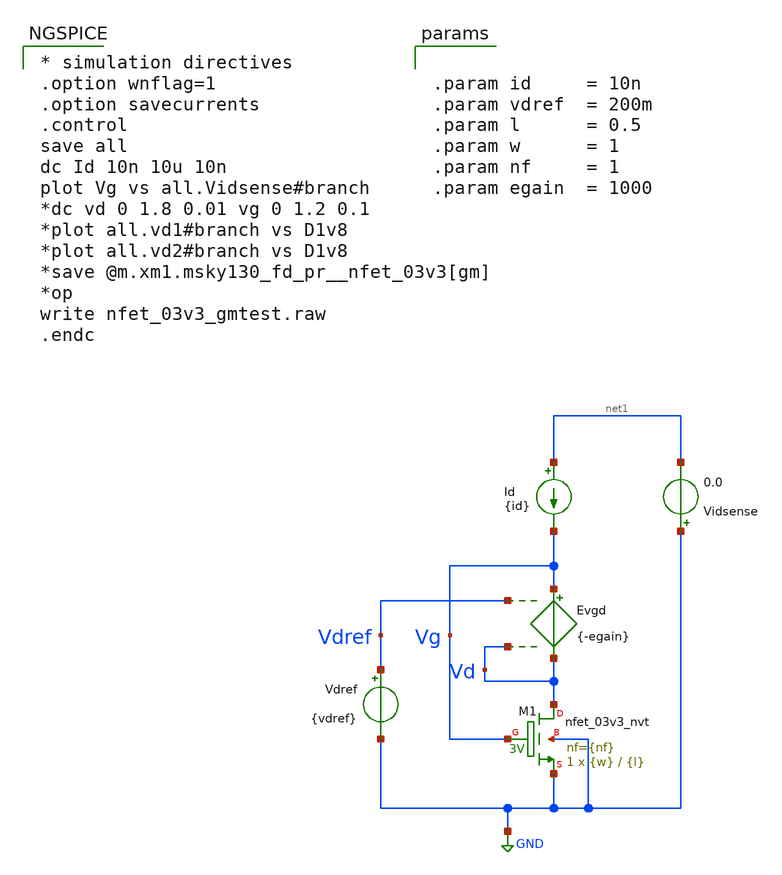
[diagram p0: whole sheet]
** sch_path: xschem/nfet_03v3_gmtest.sch
**.subckt nfet_03v3_gmtest
XM1 Vd Vg GND GND sky130_fd_pr__nfet_03v3_nvt L={l} W={w} nf={nf} ad='int((nf+1)/2) * W/nf * 0.29' as='int((nf+2)/2) * W/nf * 0.29'
+ pd='2*int((nf+1)/2) * (W/nf + 0.29)' ps='2*int((nf+2)/2) * (W/nf + 0.29)' nrd='0.29 / W' nrs='0.29 / W'
+ sa=0 sb=0 sd=0 mult=1 m=1
Evgd Vg Vd Vdref Vd {-egain}
Id net1 Vg {id}
Vdref Vdref GND {vdref}
Vidsense GND net1 0.0
**** begin user architecture code

** opencircuitdesign pdks install
.lib $::SKYWATER_MODELS/sky130.lib.spice tt



* simulation directives
.option wnflag=1
.option savecurrents
.control
save all
dc Id 10n 10u 10n
plot Vg vs all.Vidsense#branch
*dc vd 0 1.8 0.01 vg 0 1.2 0.1
*plot all.vd1#branch vs D1v8
*plot all.vd2#branch vs D1v8
*save @m.xm1.msky130_fd_pr__nfet_03v3[gm]
*op
write nfet_03v3_gmtest.raw
.endc




.param id     = 10n
.param vdref  = 200m
.param l      = 0.5
.param w      = 1
.param nf     = 1
.param egain  = 1000


**** end user architecture code
**.ends
.GLOBAL GND
.end
